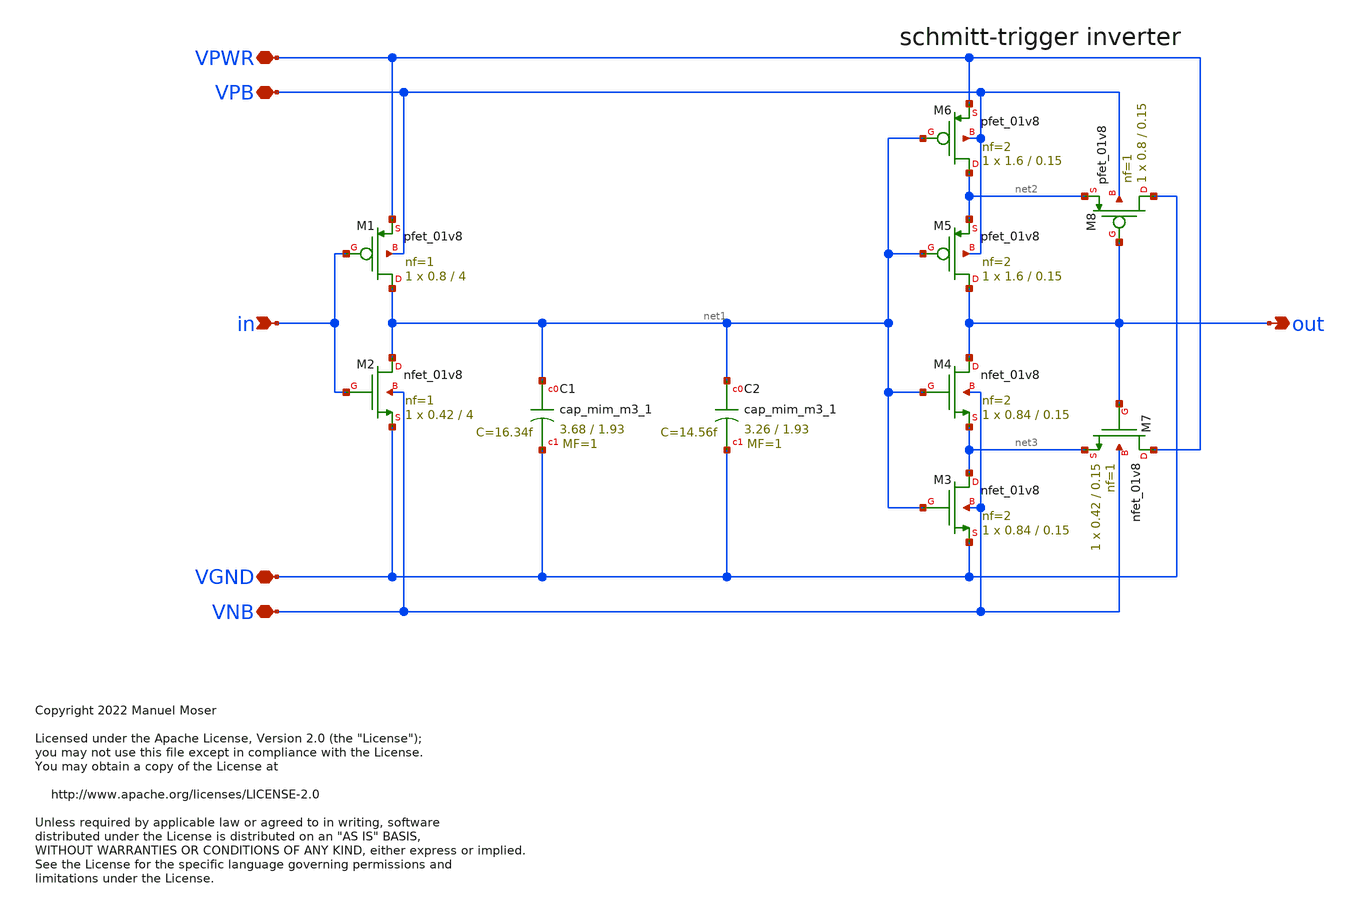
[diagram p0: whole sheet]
** sch_path: xschem/delay_macrocell/delay_macrocell.sch
* Copyright 2022 Manuel Moser
* Licensed under the Apache License, Version 2.0 (the "License");
**.subckt delay_macrocell VPWR VGND in out VPB VNB
*.iopin VPWR
*.iopin VGND
*.ipin in
*.opin out
*.iopin VPB
*.iopin VNB
XM2 net1 in VGND VNB sky130_fd_pr__nfet_01v8 L=4 W=0.42 nf=1 ad='int((nf+1)/2) * W/nf * 0.29' as='int((nf+2)/2) * W/nf * 0.29'
+ pd='2*int((nf+1)/2) * (W/nf + 0.29)' ps='2*int((nf+2)/2) * (W/nf + 0.29)' nrd='0.29 / W' nrs='0.29 / W'
+ sa=0 sb=0 sd=0 mult=1 m=1
XM3 net3 net1 VGND VNB sky130_fd_pr__nfet_01v8 L=0.15 W=0.84 nf=2 ad='int((nf+1)/2) * W/nf * 0.29' as='int((nf+2)/2) * W/nf * 0.29'
+ pd='2*int((nf+1)/2) * (W/nf + 0.29)' ps='2*int((nf+2)/2) * (W/nf + 0.29)' nrd='0.29 / W' nrs='0.29 / W'
+ sa=0 sb=0 sd=0 mult=1 m=1
XM4 out net1 net3 VNB sky130_fd_pr__nfet_01v8 L=0.15 W=0.84 nf=2 ad='int((nf+1)/2) * W/nf * 0.29' as='int((nf+2)/2) * W/nf * 0.29'
+ pd='2*int((nf+1)/2) * (W/nf + 0.29)' ps='2*int((nf+2)/2) * (W/nf + 0.29)' nrd='0.29 / W' nrs='0.29 / W'
+ sa=0 sb=0 sd=0 mult=1 m=1
XM5 out net1 net2 VPB sky130_fd_pr__pfet_01v8 L=0.15 W=1.6 nf=2 ad='int((nf+1)/2) * W/nf * 0.29' as='int((nf+2)/2) * W/nf * 0.29'
+ pd='2*int((nf+1)/2) * (W/nf + 0.29)' ps='2*int((nf+2)/2) * (W/nf + 0.29)' nrd='0.29 / W' nrs='0.29 / W'
+ sa=0 sb=0 sd=0 mult=1 m=1
XM6 net2 net1 VPWR VPB sky130_fd_pr__pfet_01v8 L=0.15 W=1.6 nf=2 ad='int((nf+1)/2) * W/nf * 0.29' as='int((nf+2)/2) * W/nf * 0.29'
+ pd='2*int((nf+1)/2) * (W/nf + 0.29)' ps='2*int((nf+2)/2) * (W/nf + 0.29)' nrd='0.29 / W' nrs='0.29 / W'
+ sa=0 sb=0 sd=0 mult=1 m=1
XM7 VPWR out net3 VNB sky130_fd_pr__nfet_01v8 L=0.15 W=0.42 nf=1 ad='int((nf+1)/2) * W/nf * 0.29' as='int((nf+2)/2) * W/nf * 0.29'
+ pd='2*int((nf+1)/2) * (W/nf + 0.29)' ps='2*int((nf+2)/2) * (W/nf + 0.29)' nrd='0.29 / W' nrs='0.29 / W'
+ sa=0 sb=0 sd=0 mult=1 m=1
XM8 VGND out net2 VPB sky130_fd_pr__pfet_01v8 L=0.15 W=0.8 nf=1 ad='int((nf+1)/2) * W/nf * 0.29' as='int((nf+2)/2) * W/nf * 0.29'
+ pd='2*int((nf+1)/2) * (W/nf + 0.29)' ps='2*int((nf+2)/2) * (W/nf + 0.29)' nrd='0.29 / W' nrs='0.29 / W'
+ sa=0 sb=0 sd=0 mult=1 m=1
XM1 net1 in VPWR VPB sky130_fd_pr__pfet_01v8 L=4 W=0.8 nf=1 ad='int((nf+1)/2) * W/nf * 0.29' as='int((nf+2)/2) * W/nf * 0.29'
+ pd='2*int((nf+1)/2) * (W/nf + 0.29)' ps='2*int((nf+2)/2) * (W/nf + 0.29)' nrd='0.29 / W' nrs='0.29 / W'
+ sa=0 sb=0 sd=0 mult=1 m=1
XC1 net1 VGND sky130_fd_pr__cap_mim_m3_1 W=3.68 L=1.93 MF=1 m=1
XC2 net1 VGND sky130_fd_pr__cap_mim_m3_1 W=3.26 L=1.93 MF=1 m=1
**.ends
.end
